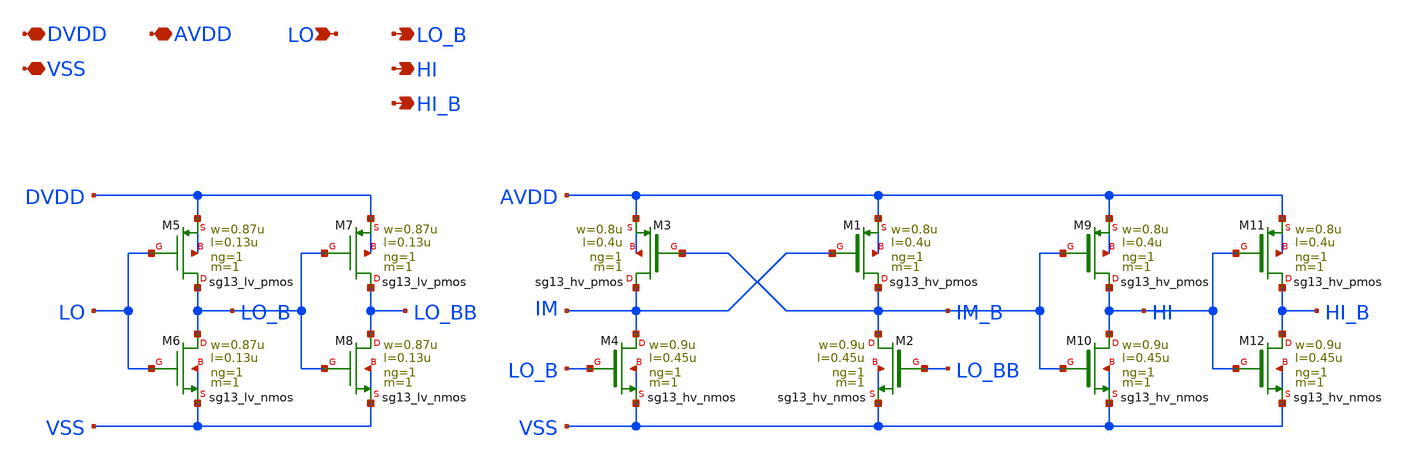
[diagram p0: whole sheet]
** sch_path: xschem/level_shifter_alt.sch
**.subckt level_shifter_alt DVDD VSS AVDD LO LO_B HI HI_B
*.iopin DVDD
*.iopin VSS
*.iopin AVDD
*.ipin LO
*.opin LO_B
*.opin HI
*.opin HI_B
XM1 IM_B IM AVDD AVDD sg13_hv_pmos w=0.8u l=0.4u ng=1 m=1 mm_ok=1
XM2 IM_B LO_BB VSS VSS sg13_hv_nmos w=0.9u l=0.45u ng=1 m=1 mm_ok=1
XM3 IM IM_B AVDD AVDD sg13_hv_pmos w=0.8u l=0.4u ng=1 m=1 mm_ok=1
XM4 IM LO_B VSS VSS sg13_hv_nmos w=0.9u l=0.45u ng=1 m=1 mm_ok=1
XM5 LO_B LO DVDD DVDD sg13_lv_pmos w=0.87u l=0.13u ng=1 m=1 mm_ok=1
XM6 LO_B LO VSS VSS sg13_lv_nmos w=0.87u l=0.13u ng=1 m=1 mm_ok=1
XM7 LO_BB LO_B DVDD DVDD sg13_lv_pmos w=0.87u l=0.13u ng=1 m=1 mm_ok=1
XM8 LO_BB LO_B VSS VSS sg13_lv_nmos w=0.87u l=0.13u ng=1 m=1 mm_ok=1
XM9 HI IM_B AVDD AVDD sg13_hv_pmos w=0.8u l=0.4u ng=1 m=1 mm_ok=1
XM10 HI IM_B VSS VSS sg13_hv_nmos w=0.9u l=0.45u ng=1 m=1 mm_ok=1
XM11 HI_B HI AVDD AVDD sg13_hv_pmos w=0.8u l=0.4u ng=1 m=1 mm_ok=1
XM12 HI_B HI VSS VSS sg13_hv_nmos w=0.9u l=0.45u ng=1 m=1 mm_ok=1
**.ends
.end
